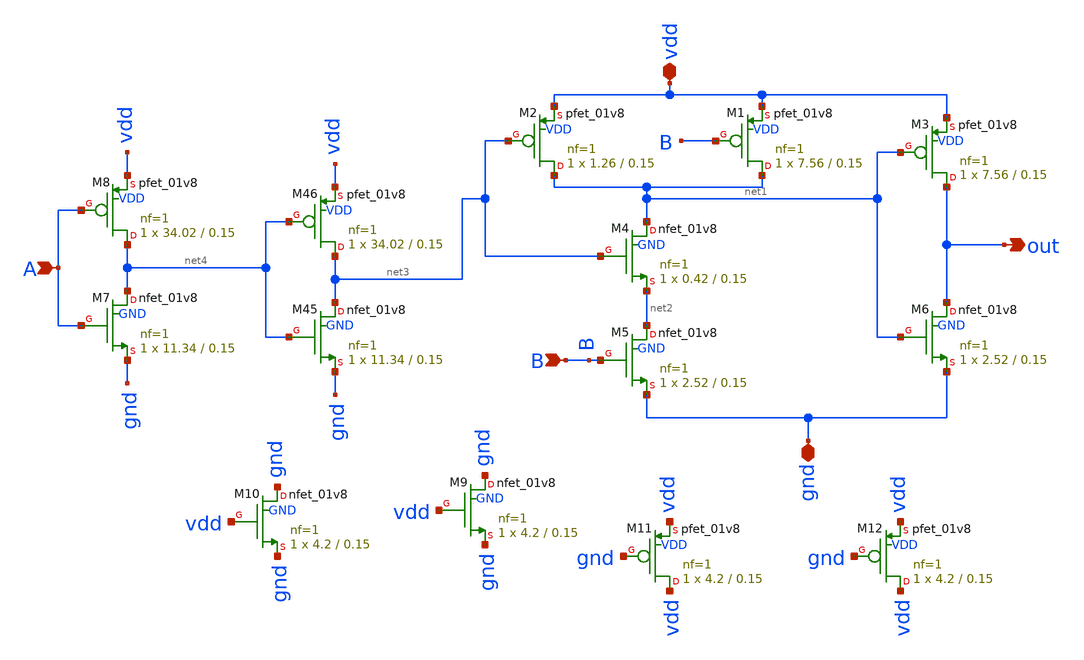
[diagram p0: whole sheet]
** sch_path: xschem/charge_pumps2/and_20x_wide.sch
**.subckt and_20x_wide gnd vdd A B out
*.iopin gnd
*.iopin vdd
*.ipin A
*.ipin B
*.opin out
XM2 net1 net3 vdd VDD sky130_fd_pr__pfet_01v8 L=0.15 W=1.26 nf=1 ad='int((nf+1)/2) * W/nf * 0.29' as='int((nf+2)/2) * W/nf * 0.29'
+ pd='2*int((nf+1)/2) * (W/nf + 0.29)' ps='2*int((nf+2)/2) * (W/nf + 0.29)' nrd='0.29 / W' nrs='0.29 / W'
+ sa=0 sb=0 sd=0 mult=1 m=1
XM1 net1 B vdd VDD sky130_fd_pr__pfet_01v8 L=0.15 W=7.56 nf=1 ad='int((nf+1)/2) * W/nf * 0.29' as='int((nf+2)/2) * W/nf * 0.29'
+ pd='2*int((nf+1)/2) * (W/nf + 0.29)' ps='2*int((nf+2)/2) * (W/nf + 0.29)' nrd='0.29 / W' nrs='0.29 / W'
+ sa=0 sb=0 sd=0 mult=1 m=1
XM3 out net1 vdd VDD sky130_fd_pr__pfet_01v8 L=0.15 W=7.56 nf=1 ad='int((nf+1)/2) * W/nf * 0.29' as='int((nf+2)/2) * W/nf * 0.29'
+ pd='2*int((nf+1)/2) * (W/nf + 0.29)' ps='2*int((nf+2)/2) * (W/nf + 0.29)' nrd='0.29 / W' nrs='0.29 / W'
+ sa=0 sb=0 sd=0 mult=1 m=1
XM4 net1 net3 net2 GND sky130_fd_pr__nfet_01v8 L=0.15 W=0.42 nf=1 ad='int((nf+1)/2) * W/nf * 0.29' as='int((nf+2)/2) * W/nf * 0.29'
+ pd='2*int((nf+1)/2) * (W/nf + 0.29)' ps='2*int((nf+2)/2) * (W/nf + 0.29)' nrd='0.29 / W' nrs='0.29 / W'
+ sa=0 sb=0 sd=0 mult=1 m=1
XM5 net2 B gnd GND sky130_fd_pr__nfet_01v8 L=0.15 W=2.52 nf=1 ad='int((nf+1)/2) * W/nf * 0.29' as='int((nf+2)/2) * W/nf * 0.29'
+ pd='2*int((nf+1)/2) * (W/nf + 0.29)' ps='2*int((nf+2)/2) * (W/nf + 0.29)' nrd='0.29 / W' nrs='0.29 / W'
+ sa=0 sb=0 sd=0 mult=1 m=1
XM6 out net1 gnd GND sky130_fd_pr__nfet_01v8 L=0.15 W=2.52 nf=1 ad='int((nf+1)/2) * W/nf * 0.29' as='int((nf+2)/2) * W/nf * 0.29'
+ pd='2*int((nf+1)/2) * (W/nf + 0.29)' ps='2*int((nf+2)/2) * (W/nf + 0.29)' nrd='0.29 / W' nrs='0.29 / W'
+ sa=0 sb=0 sd=0 mult=1 m=1
XM45 net3 net4 gnd GND sky130_fd_pr__nfet_01v8 L=0.15 W=11.34 nf=1 ad='int((nf+1)/2) * W/nf * 0.29' as='int((nf+2)/2) * W/nf * 0.29'
+ pd='2*int((nf+1)/2) * (W/nf + 0.29)' ps='2*int((nf+2)/2) * (W/nf + 0.29)' nrd='0.29 / W' nrs='0.29 / W'
+ sa=0 sb=0 sd=0 mult=1 m=1
XM46 net3 net4 vdd VDD sky130_fd_pr__pfet_01v8 L=0.15 W=34.02 nf=1 ad='int((nf+1)/2) * W/nf * 0.29' as='int((nf+2)/2) * W/nf * 0.29'
+ pd='2*int((nf+1)/2) * (W/nf + 0.29)' ps='2*int((nf+2)/2) * (W/nf + 0.29)' nrd='0.29 / W' nrs='0.29 / W'
+ sa=0 sb=0 sd=0 mult=1 m=1
XM7 net4 A gnd GND sky130_fd_pr__nfet_01v8 L=0.15 W=11.34 nf=1 ad='int((nf+1)/2) * W/nf * 0.29' as='int((nf+2)/2) * W/nf * 0.29'
+ pd='2*int((nf+1)/2) * (W/nf + 0.29)' ps='2*int((nf+2)/2) * (W/nf + 0.29)' nrd='0.29 / W' nrs='0.29 / W'
+ sa=0 sb=0 sd=0 mult=1 m=1
XM8 net4 A vdd VDD sky130_fd_pr__pfet_01v8 L=0.15 W=34.02 nf=1 ad='int((nf+1)/2) * W/nf * 0.29' as='int((nf+2)/2) * W/nf * 0.29'
+ pd='2*int((nf+1)/2) * (W/nf + 0.29)' ps='2*int((nf+2)/2) * (W/nf + 0.29)' nrd='0.29 / W' nrs='0.29 / W'
+ sa=0 sb=0 sd=0 mult=1 m=1
XM9 gnd vdd gnd GND sky130_fd_pr__nfet_01v8 L=0.15 W=4.2 nf=1 ad='int((nf+1)/2) * W/nf * 0.29' as='int((nf+2)/2) * W/nf * 0.29'
+ pd='2*int((nf+1)/2) * (W/nf + 0.29)' ps='2*int((nf+2)/2) * (W/nf + 0.29)' nrd='0.29 / W' nrs='0.29 / W'
+ sa=0 sb=0 sd=0 mult=1 m=1
XM10 gnd vdd gnd GND sky130_fd_pr__nfet_01v8 L=0.15 W=4.2 nf=1 ad='int((nf+1)/2) * W/nf * 0.29' as='int((nf+2)/2) * W/nf * 0.29'
+ pd='2*int((nf+1)/2) * (W/nf + 0.29)' ps='2*int((nf+2)/2) * (W/nf + 0.29)' nrd='0.29 / W' nrs='0.29 / W'
+ sa=0 sb=0 sd=0 mult=1 m=1
XM11 vdd gnd vdd VDD sky130_fd_pr__pfet_01v8 L=0.15 W=4.2 nf=1 ad='int((nf+1)/2) * W/nf * 0.29' as='int((nf+2)/2) * W/nf * 0.29'
+ pd='2*int((nf+1)/2) * (W/nf + 0.29)' ps='2*int((nf+2)/2) * (W/nf + 0.29)' nrd='0.29 / W' nrs='0.29 / W'
+ sa=0 sb=0 sd=0 mult=1 m=1
XM12 vdd gnd vdd VDD sky130_fd_pr__pfet_01v8 L=0.15 W=4.2 nf=1 ad='int((nf+1)/2) * W/nf * 0.29' as='int((nf+2)/2) * W/nf * 0.29'
+ pd='2*int((nf+1)/2) * (W/nf + 0.29)' ps='2*int((nf+2)/2) * (W/nf + 0.29)' nrd='0.29 / W' nrs='0.29 / W'
+ sa=0 sb=0 sd=0 mult=1 m=1
**.ends
.end
